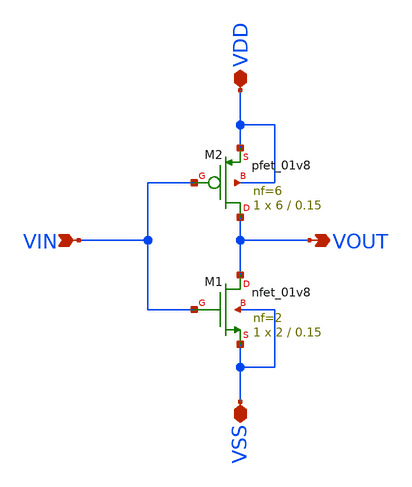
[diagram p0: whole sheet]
** sch_path: inv_2_jm.sch
**.subckt inv_2_jm VIN VOUT VDD VSS
*.ipin VIN
*.opin VOUT
*.iopin VDD
*.iopin VSS
XM1 VOUT VIN VSS VSS sky130_fd_pr__nfet_01v8 L=0.15 W=2 nf=2 ad='int((nf+1)/2) * W/nf * 0.29' as='int((nf+2)/2) * W/nf * 0.29'
+ pd='2*int((nf+1)/2) * (W/nf + 0.29)' ps='2*int((nf+2)/2) * (W/nf + 0.29)' nrd='0.29 / W' nrs='0.29 / W'
+ sa=0 sb=0 sd=0 mult=1 m=1
XM2 VOUT VIN VDD VDD sky130_fd_pr__pfet_01v8 L=0.15 W=6 nf=6 ad='int((nf+1)/2) * W/nf * 0.29' as='int((nf+2)/2) * W/nf * 0.29'
+ pd='2*int((nf+1)/2) * (W/nf + 0.29)' ps='2*int((nf+2)/2) * (W/nf + 0.29)' nrd='0.29 / W' nrs='0.29 / W'
+ sa=0 sb=0 sd=0 mult=1 m=1
**.ends
.end
